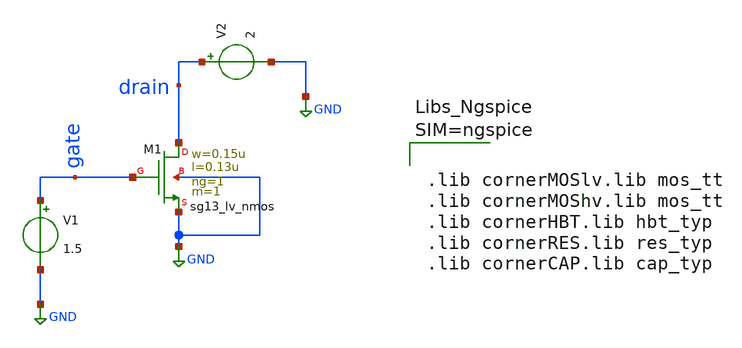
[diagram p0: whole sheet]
** sch_path: MOS_characteristics.sch
**.subckt MOS_characteristics
XM1 drain gate GND GND sg13_lv_nmos w=0.15u l=0.13u ng=1 m=1 mm_ok=1
V1 gate GND 1.5
V2 drain GND 2
**** begin user architecture code



.lib cornerMOSlv.lib mos_tt
.lib cornerMOShv.lib mos_tt
.lib cornerHBT.lib hbt_typ
.lib cornerRES.lib res_typ
.lib cornerCAP.lib cap_typ



**** end user architecture code
**.ends
.GLOBAL GND
.end
